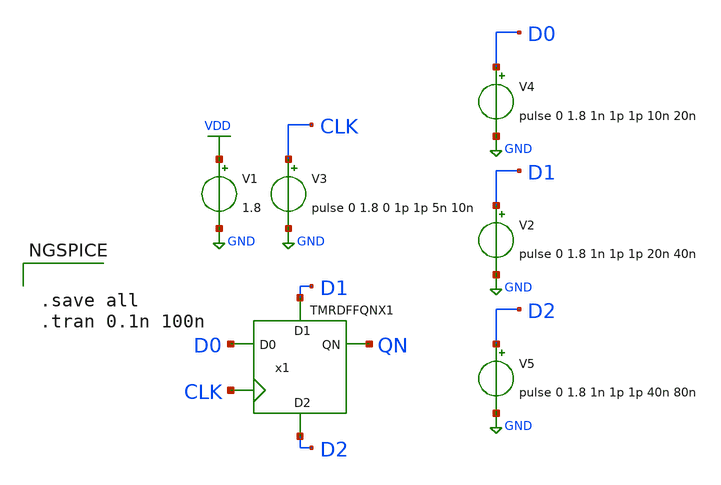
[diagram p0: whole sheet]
** sch_path: lib/xschem/test_TMRDFFQNX1.sch
**.subckt test_TMRDFFQNX1
V1 VDD GND 1.8
V3 CLK GND pulse 0 1.8 0 1p 1p 5n 10n
V4 D0 GND pulse 0 1.8 1n 1p 1p 10n 20n
V2 D1 GND pulse 0 1.8 1n 1p 1p 20n 40n
V5 D2 GND pulse 0 1.8 1n 1p 1p 40n 80n
x1 QN D0 CLK D1 D2 VDD GND TMRDFFQNX1
**** begin user architecture code

.lib $::SKYWATER_MODELS/sky130.lib.spice tt


**** end user architecture code
**.ends

* expanding   symbol:  TMRDFFQNX1.sym # of pins=5
** sym_path: lib/xschem/TMRDFFQNX1.sym
** sch_path: lib/xschem/TMRDFFQNX1.sch
.subckt TMRDFFQNX1 QN D0 CLK D1 D2 VDD VSS
*.ipin D0
*.ipin CLK
*.opin QN
*.ipin D1
*.ipin D2
x1 net3 net2 net1 QN VDD VSS VOTERN3X1
x2 CLK net3 D0 VDD VSS DFFQNX1
x3 CLK net2 D1 VDD VSS DFFQNX1
x4 CLK net1 D2 VDD VSS DFFQNX1
.ends


* expanding   symbol:  VOTERN3X1.sym # of pins=4
** sym_path: VOTERN3X1.sym
** sch_path: VOTERN3X1.sch
.subckt VOTERN3X1 A B C YN VDD VSS
*.opin YN
*.ipin A
*.ipin B
*.ipin C
XM2 net1 A VDD VDD sky130_fd_pr__pfet_01v8 L=0.15 W=2 nf=1 ad='int((nf+1)/2) * W/nf * 0.29' as='int((nf+2)/2) * W/nf * 0.29'
+ pd='2*int((nf+1)/2) * (W/nf + 0.29)' ps='2*int((nf+2)/2) * (W/nf + 0.29)' nrd='0.29 / W' nrs='0.29 / W'
+ sa=0 sb=0 sd=0 mult=2 m=2
XM3 net2 B VSS VSS sky130_fd_pr__nfet_01v8 L=0.15 W=3 nf=1 ad='int((nf+1)/2) * W/nf * 0.29' as='int((nf+2)/2) * W/nf * 0.29'
+ pd='2*int((nf+1)/2) * (W/nf + 0.29)' ps='2*int((nf+2)/2) * (W/nf + 0.29)' nrd='0.29 / W' nrs='0.29 / W'
+ sa=0 sb=0 sd=0 mult=1 m=1
XM4 YN A net2 VSS sky130_fd_pr__nfet_01v8 L=0.15 W=3 nf=1 ad='int((nf+1)/2) * W/nf * 0.29' as='int((nf+2)/2) * W/nf * 0.29'
+ pd='2*int((nf+1)/2) * (W/nf + 0.29)' ps='2*int((nf+2)/2) * (W/nf + 0.29)' nrd='0.29 / W' nrs='0.29 / W'
+ sa=0 sb=0 sd=0 mult=1 m=1
XM1 net1 B VDD VDD sky130_fd_pr__pfet_01v8 L=0.15 W=2 nf=1 ad='int((nf+1)/2) * W/nf * 0.29' as='int((nf+2)/2) * W/nf * 0.29'
+ pd='2*int((nf+1)/2) * (W/nf + 0.29)' ps='2*int((nf+2)/2) * (W/nf + 0.29)' nrd='0.29 / W' nrs='0.29 / W'
+ sa=0 sb=0 sd=0 mult=2 m=2
XM5 net3 B net1 VDD sky130_fd_pr__pfet_01v8 L=0.15 W=2 nf=1 ad='int((nf+1)/2) * W/nf * 0.29' as='int((nf+2)/2) * W/nf * 0.29'
+ pd='2*int((nf+1)/2) * (W/nf + 0.29)' ps='2*int((nf+2)/2) * (W/nf + 0.29)' nrd='0.29 / W' nrs='0.29 / W'
+ sa=0 sb=0 sd=0 mult=2 m=2
XM6 YN C net3 VDD sky130_fd_pr__pfet_01v8 L=0.15 W=2 nf=1 ad='int((nf+1)/2) * W/nf * 0.29' as='int((nf+2)/2) * W/nf * 0.29'
+ pd='2*int((nf+1)/2) * (W/nf + 0.29)' ps='2*int((nf+2)/2) * (W/nf + 0.29)' nrd='0.29 / W' nrs='0.29 / W'
+ sa=0 sb=0 sd=0 mult=2 m=2
XM7 net3 C net1 VDD sky130_fd_pr__pfet_01v8 L=0.15 W=2 nf=1 ad='int((nf+1)/2) * W/nf * 0.29' as='int((nf+2)/2) * W/nf * 0.29'
+ pd='2*int((nf+1)/2) * (W/nf + 0.29)' ps='2*int((nf+2)/2) * (W/nf + 0.29)' nrd='0.29 / W' nrs='0.29 / W'
+ sa=0 sb=0 sd=0 mult=2 m=2
XM10 YN A net3 VDD sky130_fd_pr__pfet_01v8 L=0.15 W=2 nf=1 ad='int((nf+1)/2) * W/nf * 0.29' as='int((nf+2)/2) * W/nf * 0.29'
+ pd='2*int((nf+1)/2) * (W/nf + 0.29)' ps='2*int((nf+2)/2) * (W/nf + 0.29)' nrd='0.29 / W' nrs='0.29 / W'
+ sa=0 sb=0 sd=0 mult=2 m=2
XM8 net4 B VSS VSS sky130_fd_pr__nfet_01v8 L=0.15 W=3 nf=1 ad='int((nf+1)/2) * W/nf * 0.29' as='int((nf+2)/2) * W/nf * 0.29'
+ pd='2*int((nf+1)/2) * (W/nf + 0.29)' ps='2*int((nf+2)/2) * (W/nf + 0.29)' nrd='0.29 / W' nrs='0.29 / W'
+ sa=0 sb=0 sd=0 mult=1 m=1
XM9 YN C net4 VSS sky130_fd_pr__nfet_01v8 L=0.15 W=3 nf=1 ad='int((nf+1)/2) * W/nf * 0.29' as='int((nf+2)/2) * W/nf * 0.29'
+ pd='2*int((nf+1)/2) * (W/nf + 0.29)' ps='2*int((nf+2)/2) * (W/nf + 0.29)' nrd='0.29 / W' nrs='0.29 / W'
+ sa=0 sb=0 sd=0 mult=1 m=1
XM11 net5 C VSS VSS sky130_fd_pr__nfet_01v8 L=0.15 W=3 nf=1 ad='int((nf+1)/2) * W/nf * 0.29' as='int((nf+2)/2) * W/nf * 0.29'
+ pd='2*int((nf+1)/2) * (W/nf + 0.29)' ps='2*int((nf+2)/2) * (W/nf + 0.29)' nrd='0.29 / W' nrs='0.29 / W'
+ sa=0 sb=0 sd=0 mult=1 m=1
XM12 YN A net5 VSS sky130_fd_pr__nfet_01v8 L=0.15 W=3 nf=1 ad='int((nf+1)/2) * W/nf * 0.29' as='int((nf+2)/2) * W/nf * 0.29'
+ pd='2*int((nf+1)/2) * (W/nf + 0.29)' ps='2*int((nf+2)/2) * (W/nf + 0.29)' nrd='0.29 / W' nrs='0.29 / W'
+ sa=0 sb=0 sd=0 mult=1 m=1
.ends


* expanding   symbol:  DFFQNX1.sym # of pins=3
** sym_path: DFFQNX1.sym
** sch_path: DFFQNX1.sch
.subckt DFFQNX1 CLK QN D VDD VSS
*.ipin CLK
*.ipin D
*.opin QN
x1 B1 C1 CLK A1 NAND3X1
x2 A1 B1 D NAND2X1
x3 D1 A1 C1 NAND2X1
x4 C1 D1 CLK NAND2X1
x5 QN B1 net1 NAND2X1
x6 net1 QN C1 NAND2X1
.ends


* expanding   symbol:  NAND3X1.sym # of pins=4
** sym_path: lib/xschem/NAND3X1.sym
** sch_path: lib/xschem/NAND3X1.sch
.subckt NAND3X1 Y A B C
*.ipin A
*.opin Y
*.ipin B
*.ipin C
XM1 net2 C GND GND sky130_fd_pr__nfet_01v8 L=0.15 W=3 nf=1 ad='int((nf+1)/2) * W/nf * 0.29' as='int((nf+2)/2) * W/nf * 0.29'
+ pd='2*int((nf+1)/2) * (W/nf + 0.29)' ps='2*int((nf+2)/2) * (W/nf + 0.29)' nrd='0.29 / W' nrs='0.29 / W'
+ sa=0 sb=0 sd=0 mult=1 m=1
XM2 Y A VDD VDD sky130_fd_pr__pfet_01v8 L=0.15 W=2 nf=1 ad='int((nf+1)/2) * W/nf * 0.29' as='int((nf+2)/2) * W/nf * 0.29'
+ pd='2*int((nf+1)/2) * (W/nf + 0.29)' ps='2*int((nf+2)/2) * (W/nf + 0.29)' nrd='0.29 / W' nrs='0.29 / W'
+ sa=0 sb=0 sd=0 mult=1 m=1
XM3 net1 B net2 GND sky130_fd_pr__nfet_01v8 L=0.15 W=3 nf=1 ad='int((nf+1)/2) * W/nf * 0.29' as='int((nf+2)/2) * W/nf * 0.29'
+ pd='2*int((nf+1)/2) * (W/nf + 0.29)' ps='2*int((nf+2)/2) * (W/nf + 0.29)' nrd='0.29 / W' nrs='0.29 / W'
+ sa=0 sb=0 sd=0 mult=1 m=1
XM4 Y A net1 GND sky130_fd_pr__nfet_01v8 L=0.15 W=3 nf=1 ad='int((nf+1)/2) * W/nf * 0.29' as='int((nf+2)/2) * W/nf * 0.29'
+ pd='2*int((nf+1)/2) * (W/nf + 0.29)' ps='2*int((nf+2)/2) * (W/nf + 0.29)' nrd='0.29 / W' nrs='0.29 / W'
+ sa=0 sb=0 sd=0 mult=1 m=1
XM5 Y A VDD VDD sky130_fd_pr__pfet_01v8 L=0.15 W=2 nf=1 ad='int((nf+1)/2) * W/nf * 0.29' as='int((nf+2)/2) * W/nf * 0.29'
+ pd='2*int((nf+1)/2) * (W/nf + 0.29)' ps='2*int((nf+2)/2) * (W/nf + 0.29)' nrd='0.29 / W' nrs='0.29 / W'
+ sa=0 sb=0 sd=0 mult=1 m=1
XM6 Y B VDD VDD sky130_fd_pr__pfet_01v8 L=0.15 W=2 nf=1 ad='int((nf+1)/2) * W/nf * 0.29' as='int((nf+2)/2) * W/nf * 0.29'
+ pd='2*int((nf+1)/2) * (W/nf + 0.29)' ps='2*int((nf+2)/2) * (W/nf + 0.29)' nrd='0.29 / W' nrs='0.29 / W'
+ sa=0 sb=0 sd=0 mult=1 m=1
XM7 Y B VDD VDD sky130_fd_pr__pfet_01v8 L=0.15 W=2 nf=1 ad='int((nf+1)/2) * W/nf * 0.29' as='int((nf+2)/2) * W/nf * 0.29'
+ pd='2*int((nf+1)/2) * (W/nf + 0.29)' ps='2*int((nf+2)/2) * (W/nf + 0.29)' nrd='0.29 / W' nrs='0.29 / W'
+ sa=0 sb=0 sd=0 mult=1 m=1
XM8 Y C VDD VDD sky130_fd_pr__pfet_01v8 L=0.15 W=2 nf=1 ad='int((nf+1)/2) * W/nf * 0.29' as='int((nf+2)/2) * W/nf * 0.29'
+ pd='2*int((nf+1)/2) * (W/nf + 0.29)' ps='2*int((nf+2)/2) * (W/nf + 0.29)' nrd='0.29 / W' nrs='0.29 / W'
+ sa=0 sb=0 sd=0 mult=1 m=1
XM9 Y C VDD VDD sky130_fd_pr__pfet_01v8 L=0.15 W=2 nf=1 ad='int((nf+1)/2) * W/nf * 0.29' as='int((nf+2)/2) * W/nf * 0.29'
+ pd='2*int((nf+1)/2) * (W/nf + 0.29)' ps='2*int((nf+2)/2) * (W/nf + 0.29)' nrd='0.29 / W' nrs='0.29 / W'
+ sa=0 sb=0 sd=0 mult=1 m=1
.ends


* expanding   symbol:  NAND2X1.sym # of pins=3
** sym_path: lib/xschem/NAND2X1.sym
** sch_path: lib/xschem/NAND2X1.sch
.subckt NAND2X1 Y A B
*.ipin A
*.opin Y
*.ipin B
XM1 Y A VDD VDD sky130_fd_pr__pfet_01v8 L=0.15 W=2 nf=1 ad='int((nf+1)/2) * W/nf * 0.29' as='int((nf+2)/2) * W/nf * 0.29'
+ pd='2*int((nf+1)/2) * (W/nf + 0.29)' ps='2*int((nf+2)/2) * (W/nf + 0.29)' nrd='0.29 / W' nrs='0.29 / W'
+ sa=0 sb=0 sd=0 mult=1 m=1
XM5 Y A net1 VSS sky130_fd_pr__nfet_01v8 L=0.15 W=3 nf=1 ad='int((nf+1)/2) * W/nf * 0.29' as='int((nf+2)/2) * W/nf * 0.29'
+ pd='2*int((nf+1)/2) * (W/nf + 0.29)' ps='2*int((nf+2)/2) * (W/nf + 0.29)' nrd='0.29 / W' nrs='0.29 / W'
+ sa=0 sb=0 sd=0 mult=1 m=1
XM2 Y A VDD VDD sky130_fd_pr__pfet_01v8 L=0.15 W=2 nf=1 ad='int((nf+1)/2) * W/nf * 0.29' as='int((nf+2)/2) * W/nf * 0.29'
+ pd='2*int((nf+1)/2) * (W/nf + 0.29)' ps='2*int((nf+2)/2) * (W/nf + 0.29)' nrd='0.29 / W' nrs='0.29 / W'
+ sa=0 sb=0 sd=0 mult=1 m=1
XM3 Y B VDD VDD sky130_fd_pr__pfet_01v8 L=0.15 W=2 nf=1 ad='int((nf+1)/2) * W/nf * 0.29' as='int((nf+2)/2) * W/nf * 0.29'
+ pd='2*int((nf+1)/2) * (W/nf + 0.29)' ps='2*int((nf+2)/2) * (W/nf + 0.29)' nrd='0.29 / W' nrs='0.29 / W'
+ sa=0 sb=0 sd=0 mult=1 m=1
XM4 Y B VDD VDD sky130_fd_pr__pfet_01v8 L=0.15 W=2 nf=1 ad='int((nf+1)/2) * W/nf * 0.29' as='int((nf+2)/2) * W/nf * 0.29'
+ pd='2*int((nf+1)/2) * (W/nf + 0.29)' ps='2*int((nf+2)/2) * (W/nf + 0.29)' nrd='0.29 / W' nrs='0.29 / W'
+ sa=0 sb=0 sd=0 mult=1 m=1
XM6 net1 B VSS VSS sky130_fd_pr__nfet_01v8 L=0.15 W=3 nf=1 ad='int((nf+1)/2) * W/nf * 0.29' as='int((nf+2)/2) * W/nf * 0.29'
+ pd='2*int((nf+1)/2) * (W/nf + 0.29)' ps='2*int((nf+2)/2) * (W/nf + 0.29)' nrd='0.29 / W' nrs='0.29 / W'
+ sa=0 sb=0 sd=0 mult=1 m=1
.ends

.GLOBAL VDD
.GLOBAL GND
**** begin user architecture code


.save all
.tran 0.1n 100n


**** end user architecture code
.end
